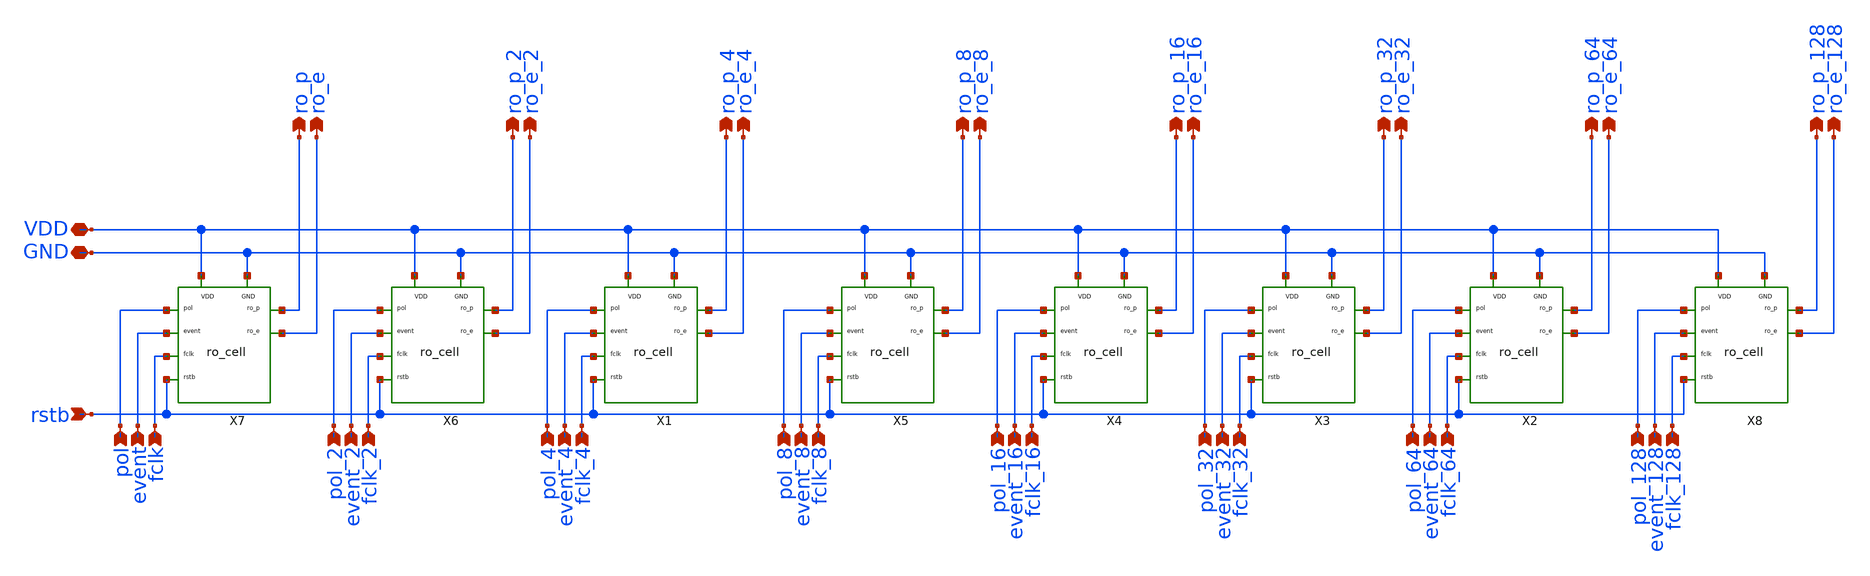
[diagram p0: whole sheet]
** sch_path: xschem/readout/ro_bank.sch
**.subckt ro_bank ro_p_4 fclk_4 event_4 pol_4 ro_e_4 ro_p_64 fclk_64 event_64 pol_64 ro_e_64 ro_p_32
*+ fclk_32 event_32 pol_32 ro_e_32 ro_p_16 fclk_16 event_16 pol_16 ro_e_16 ro_p_8 fclk_8 event_8 pol_8 ro_e_8
*+ ro_p_2 fclk_2 event_2 pol_2 ro_e_2 ro_p fclk event pol ro_e fclk_128 event_128 pol_128 ro_p_128 ro_e_128
*+ GND VDD rstb
*.opin ro_p_4
*.ipin fclk_4
*.ipin event_4
*.ipin pol_4
*.opin ro_e_4
*.opin ro_p_64
*.ipin fclk_64
*.ipin event_64
*.ipin pol_64
*.opin ro_e_64
*.opin ro_p_32
*.ipin fclk_32
*.ipin event_32
*.ipin pol_32
*.opin ro_e_32
*.opin ro_p_16
*.ipin fclk_16
*.ipin event_16
*.ipin pol_16
*.opin ro_e_16
*.opin ro_p_8
*.ipin fclk_8
*.ipin event_8
*.ipin pol_8
*.opin ro_e_8
*.opin ro_p_2
*.ipin fclk_2
*.ipin event_2
*.ipin pol_2
*.opin ro_e_2
*.opin ro_p
*.ipin fclk
*.ipin event
*.ipin pol
*.opin ro_e
*.ipin fclk_128
*.ipin event_128
*.ipin pol_128
*.opin ro_p_128
*.opin ro_e_128
*.iopin GND
*.iopin VDD
*.ipin rstb
X1 pol_4 event_4 fclk_4 rstb ro_p_4 ro_e_4 VDD GND ro_cell
X8 pol_128 event_128 fclk_128 rstb ro_p_128 ro_e_128 VDD GND ro_cell
X2 pol_64 event_64 fclk_64 rstb ro_p_64 ro_e_64 VDD GND ro_cell
X3 pol_32 event_32 fclk_32 rstb ro_p_32 ro_e_32 VDD GND ro_cell
X4 pol_16 event_16 fclk_16 rstb ro_p_16 ro_e_16 VDD GND ro_cell
X5 pol_8 event_8 fclk_8 rstb ro_p_8 ro_e_8 VDD GND ro_cell
X6 pol_2 event_2 fclk_2 rstb ro_p_2 ro_e_2 VDD GND ro_cell
X7 pol event fclk rstb ro_p ro_e VDD GND ro_cell
**.ends

* expanding   symbol:  readout/ro_cell.sym # of pins=8
** sym_path: xschem/readout/ro_cell.sym
** sch_path: xschem/readout/ro_cell.sch
.subckt ro_cell pol event fclk rstb ro_p ro_e VDD GND
*.ipin pol
*.ipin event
*.ipin fclk
*.ipin rstb
*.iopin VDD
*.iopin GND
*.opin ro_p
*.opin ro_e
x1 fclk pol rstb GND GND VDD VDD ro_p sky130_fd_sc_lp__dfrtn_1
x2 fclk event rstb GND GND VDD VDD ro_e sky130_fd_sc_lp__dfrtn_1
.ends

.end
